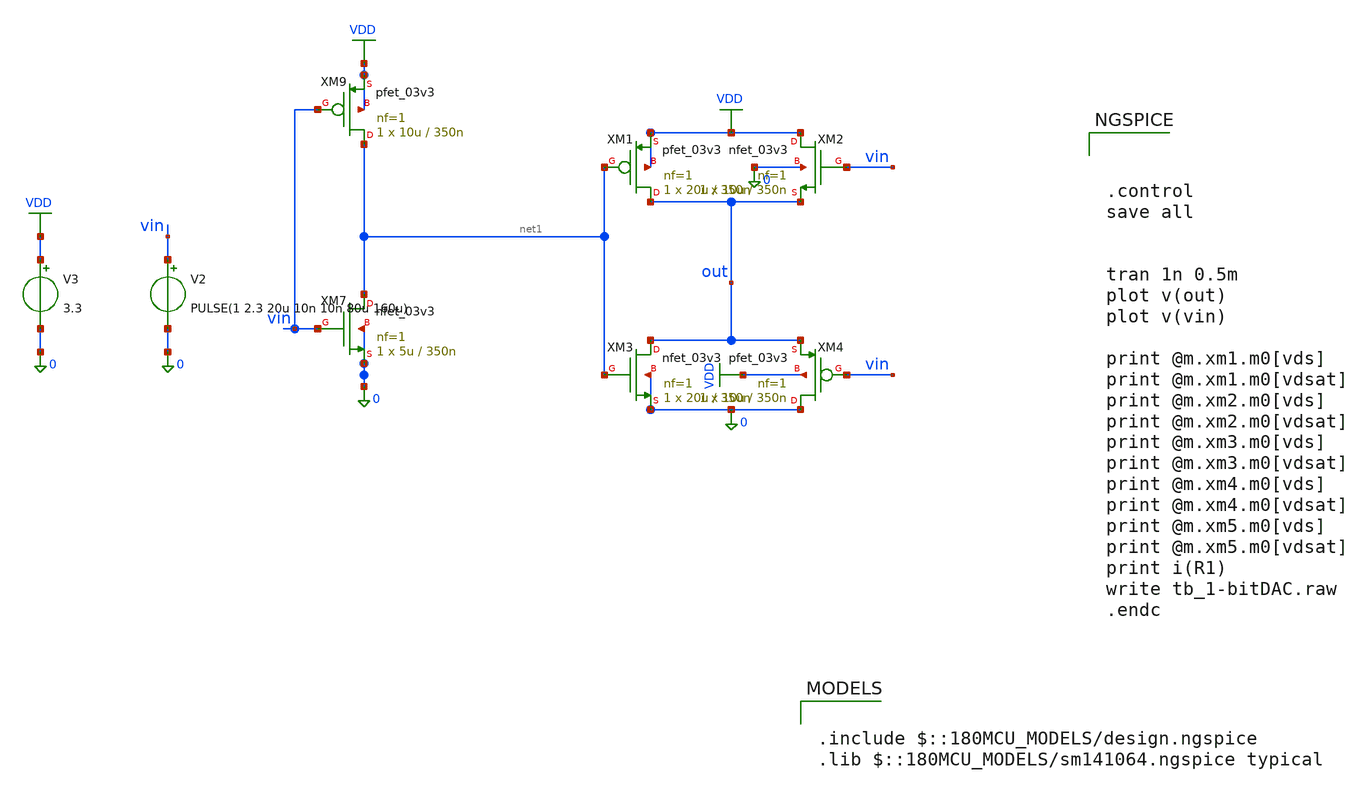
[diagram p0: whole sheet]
** sch_path: amplifier/tb_1-bitDAC_nosymbol.sch
**.subckt tb_1-bitDAC_nosymbol
V2 vin 0 PULSE(1 2.3 20u 10n 10n 80u 160u)
V3 VDD 0 3.3
XM7 net1 vin 0 0 nfet_03v3 L=350n W=5u nf=1 ad='int((nf+1)/2) * W/nf * 0.18u' as='int((nf+2)/2) * W/nf * 0.18u'
+ pd='2*int((nf+1)/2) * (W/nf + 0.18u)' ps='2*int((nf+2)/2) * (W/nf + 0.18u)' nrd='0.18u / W' nrs='0.18u / W'
+ sa=0 sb=0 sd=0 m=1
XM9 net1 vin VDD VDD pfet_03v3 L=350n W=10u nf=1 ad='int((nf+1)/2) * W/nf * 0.18u' as='int((nf+2)/2) * W/nf * 0.18u'
+ pd='2*int((nf+1)/2) * (W/nf + 0.18u)' ps='2*int((nf+2)/2) * (W/nf + 0.18u)' nrd='0.18u / W' nrs='0.18u / W'
+ sa=0 sb=0 sd=0 m=1
XM1 out net1 VDD VDD pfet_03v3 L=350n W=20u nf=1 ad='int((nf+1)/2) * W/nf * 0.18u' as='int((nf+2)/2) * W/nf * 0.18u'
+ pd='2*int((nf+1)/2) * (W/nf + 0.18u)' ps='2*int((nf+2)/2) * (W/nf + 0.18u)' nrd='0.18u / W' nrs='0.18u / W'
+ sa=0 sb=0 sd=0 m=1
XM2 VDD vin out 0 nfet_03v3 L=350n W=10u nf=1 ad='int((nf+1)/2) * W/nf * 0.18u' as='int((nf+2)/2) * W/nf * 0.18u'
+ pd='2*int((nf+1)/2) * (W/nf + 0.18u)' ps='2*int((nf+2)/2) * (W/nf + 0.18u)' nrd='0.18u / W' nrs='0.18u / W'
+ sa=0 sb=0 sd=0 m=1
XM3 out net1 0 0 nfet_03v3 L=350n W=20u nf=1 ad='int((nf+1)/2) * W/nf * 0.18u' as='int((nf+2)/2) * W/nf * 0.18u'
+ pd='2*int((nf+1)/2) * (W/nf + 0.18u)' ps='2*int((nf+2)/2) * (W/nf + 0.18u)' nrd='0.18u / W' nrs='0.18u / W'
+ sa=0 sb=0 sd=0 m=1
XM4 0 vin out VDD pfet_03v3 L=350n W=10u nf=1 ad='int((nf+1)/2) * W/nf * 0.18u' as='int((nf+2)/2) * W/nf * 0.18u'
+ pd='2*int((nf+1)/2) * (W/nf + 0.18u)' ps='2*int((nf+2)/2) * (W/nf + 0.18u)' nrd='0.18u / W' nrs='0.18u / W'
+ sa=0 sb=0 sd=0 m=1
**** begin user architecture code

.include $::180MCU_MODELS/design.ngspice
.lib $::180MCU_MODELS/sm141064.ngspice typical




.control
save all


tran 1n 0.5m
plot v(out)
plot v(vin)

print @m.xm1.m0[vds]
print @m.xm1.m0[vdsat]
print @m.xm2.m0[vds]
print @m.xm2.m0[vdsat]
print @m.xm3.m0[vds]
print @m.xm3.m0[vdsat]
print @m.xm4.m0[vds]
print @m.xm4.m0[vdsat]
print @m.xm5.m0[vds]
print @m.xm5.m0[vdsat]
print i(R1)
write tb_1-bitDAC.raw
.endc


**** end user architecture code
**.ends
.GLOBAL VDD
.end
